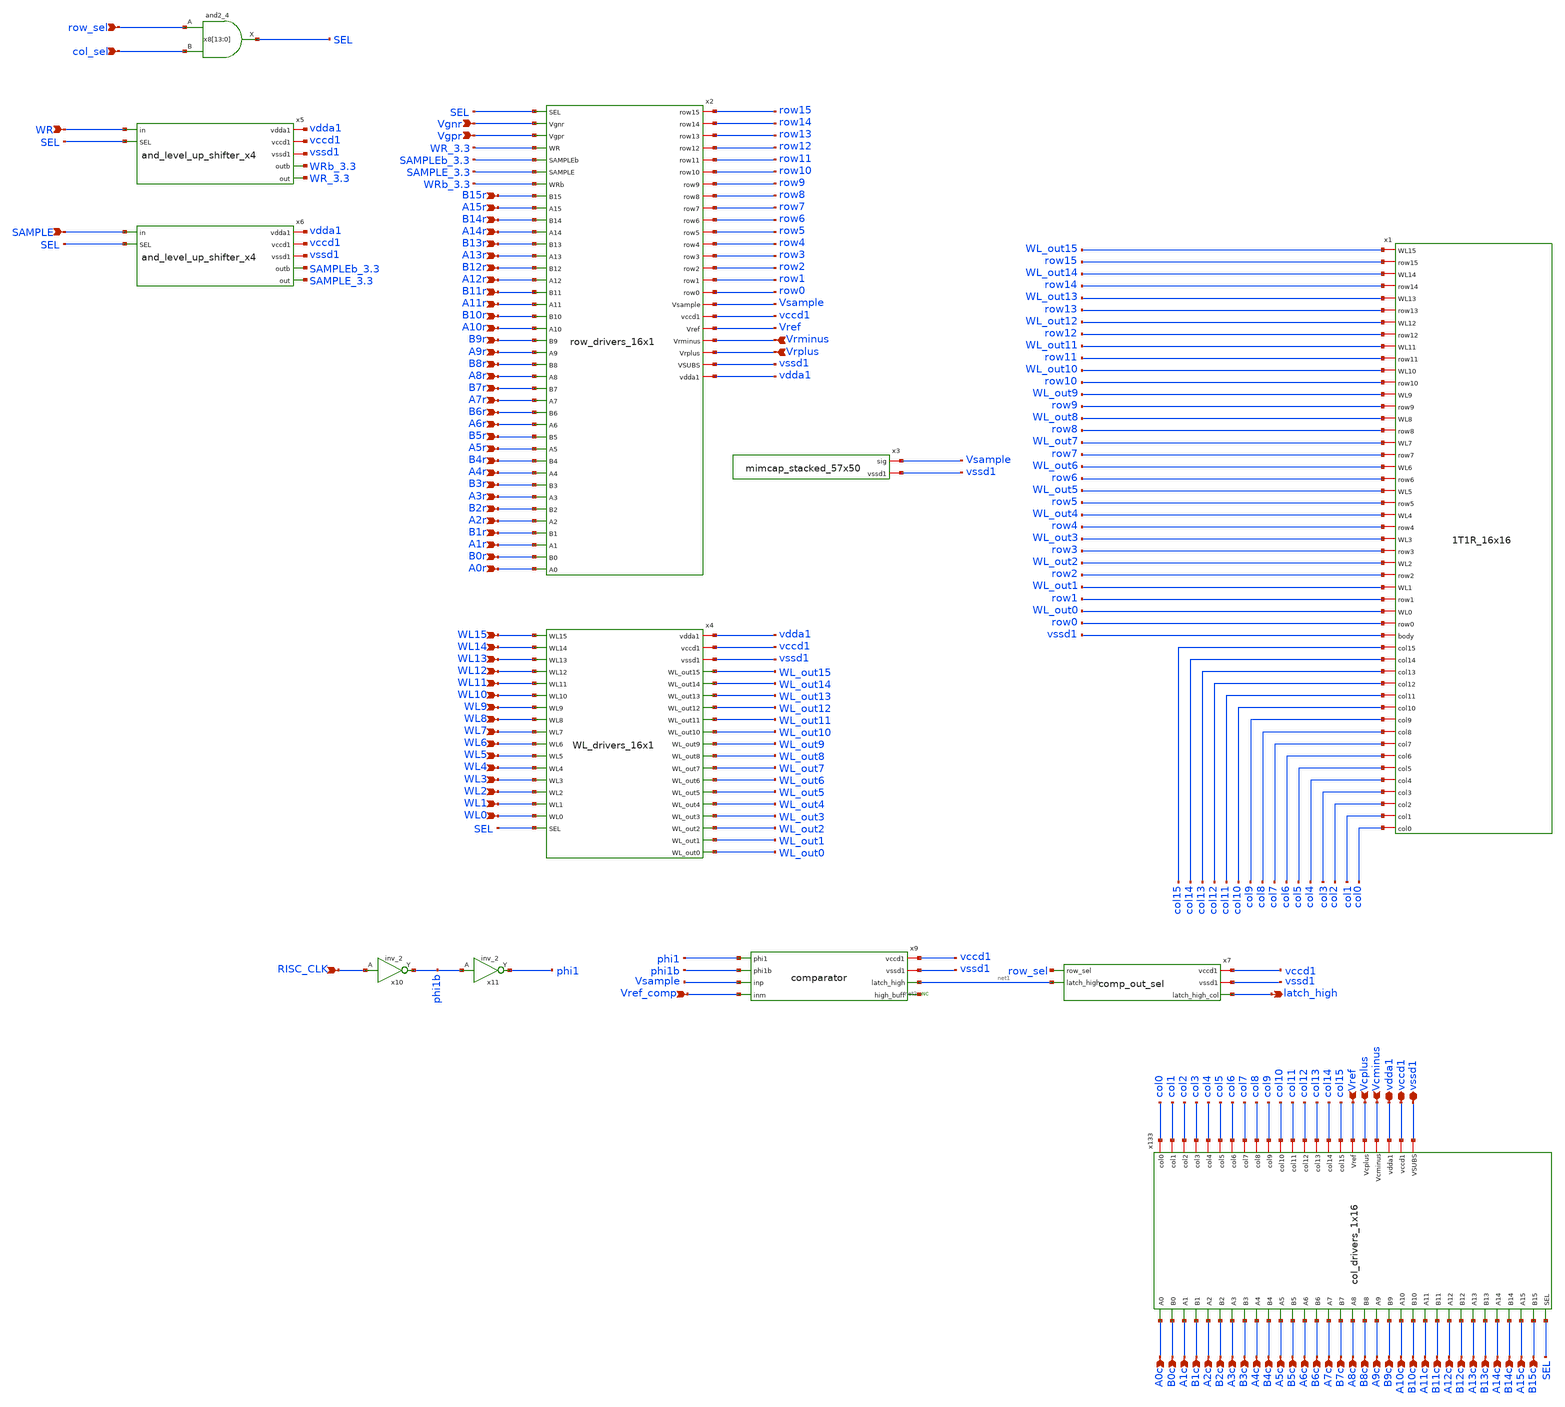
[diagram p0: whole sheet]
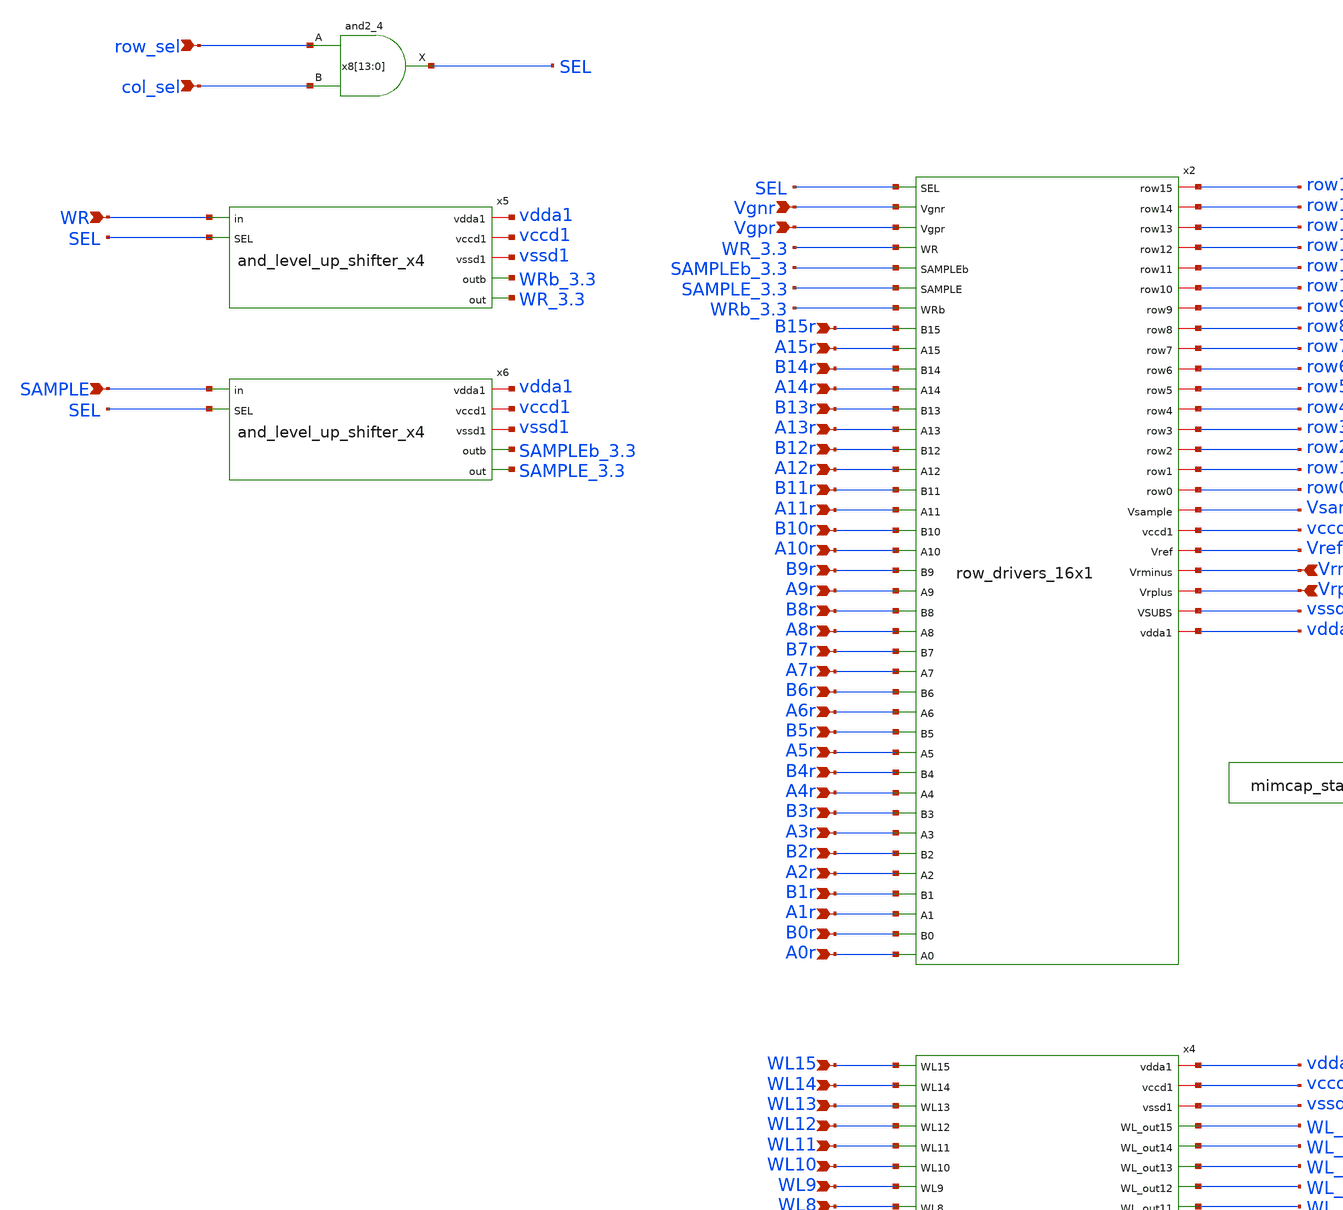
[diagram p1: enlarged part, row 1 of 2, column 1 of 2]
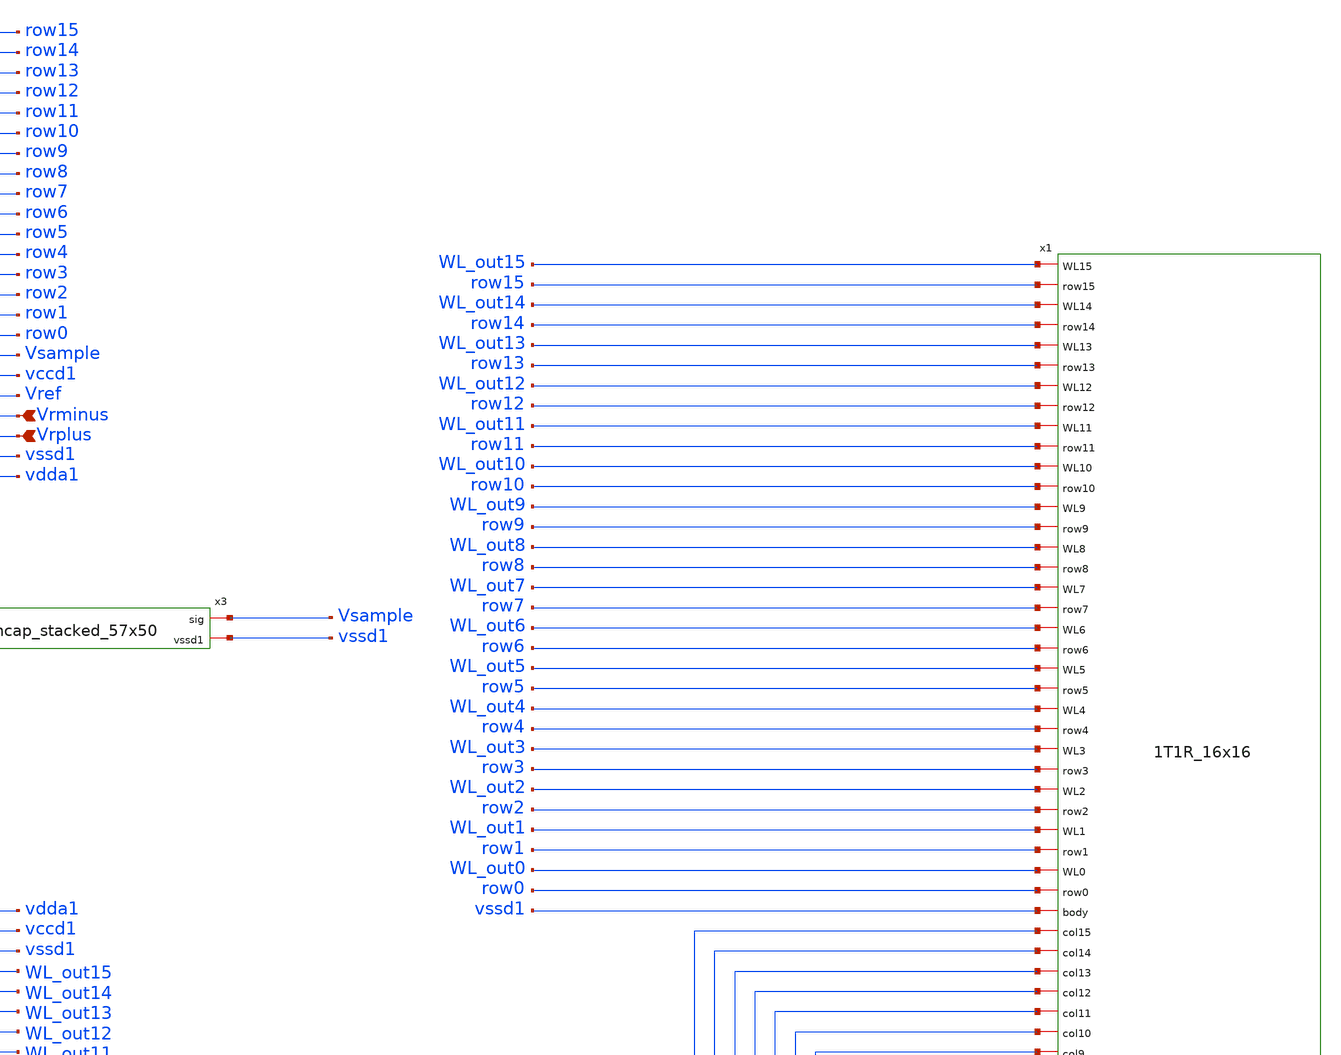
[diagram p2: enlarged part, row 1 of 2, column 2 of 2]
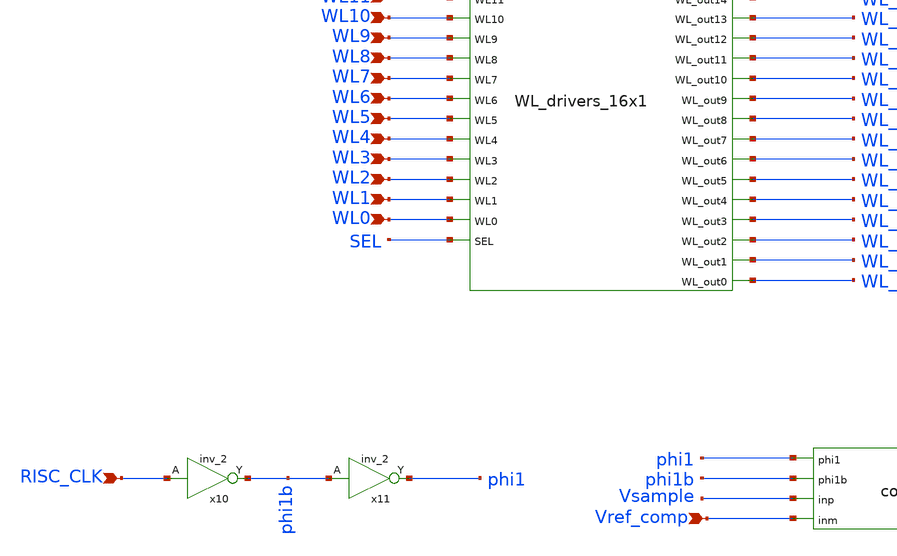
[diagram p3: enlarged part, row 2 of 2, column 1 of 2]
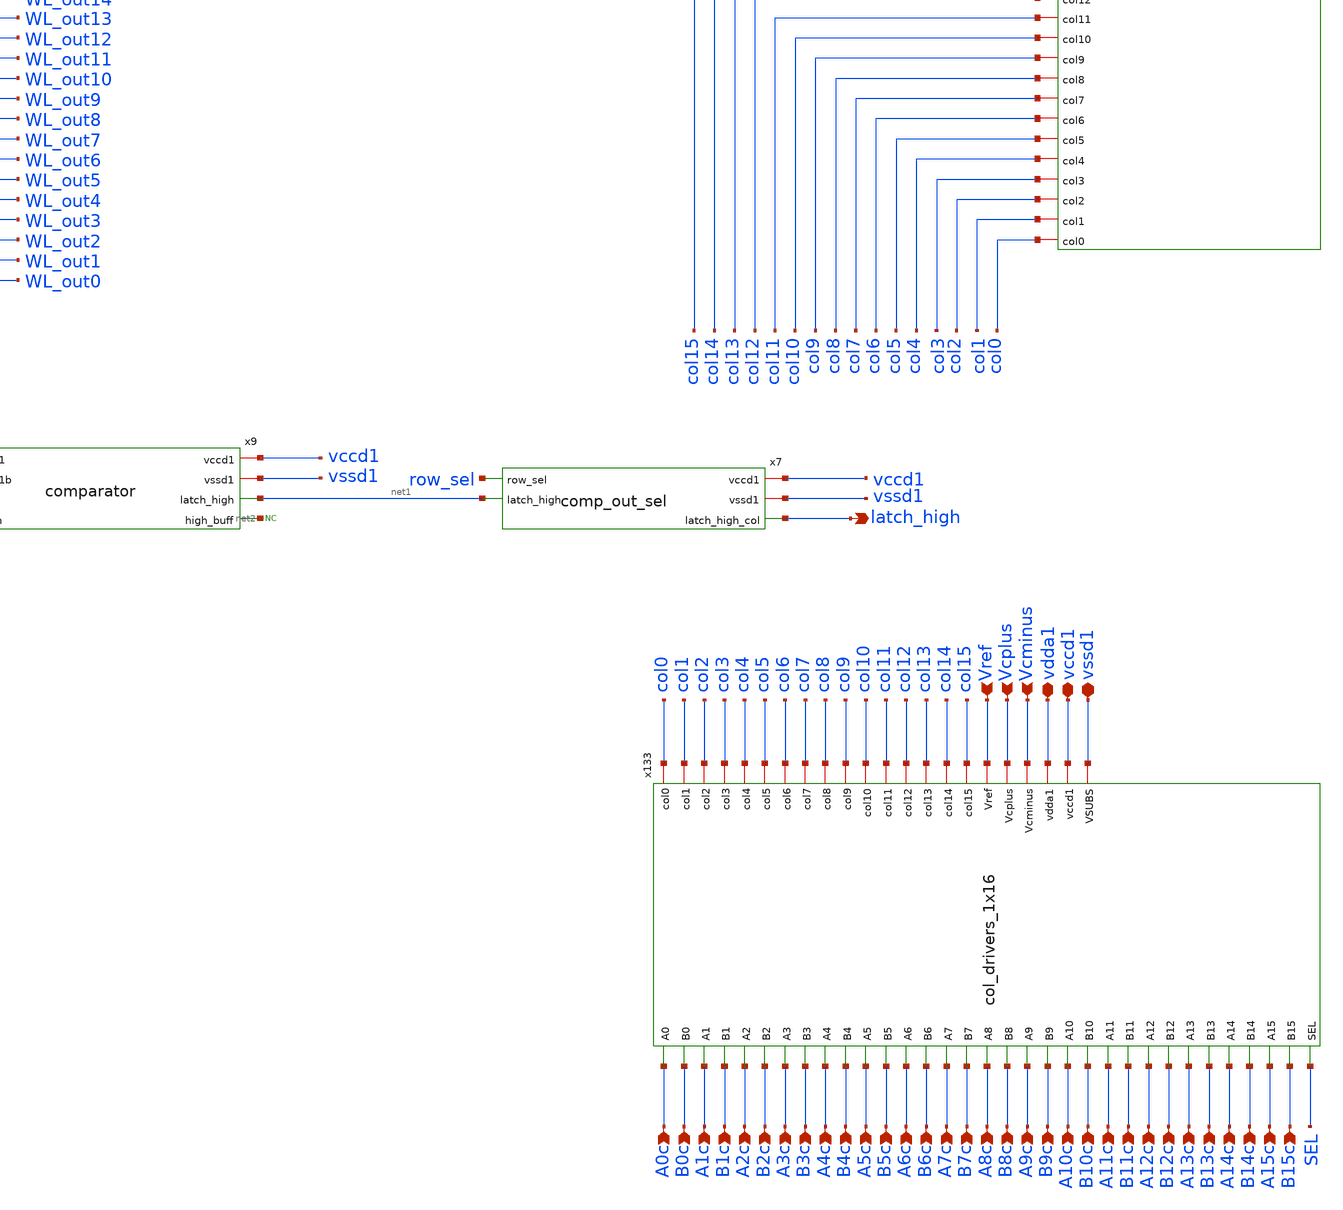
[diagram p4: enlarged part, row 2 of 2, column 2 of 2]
** sch_path: xschem/core.sch
**.subckt core vdda1 vssd1 Vref Vcplus Vcminus vccd1 Vrplus Vrminus Vgpr A0r A1r A2r A3r A4r A5r A6r
*+ A7r A8r A9r A10r A11r A12r A13r A14r A15r B0r B1r B2r B3r B4r B5r B6r B7r B8r B10r B11r B12r B13r B14r
*+ B15r B9r Vgnr A0c A1c A2c A3c A4c A5c A6c A7c A8c A9c A10c A11c A12c A13c A14c A15c B0c B1c B2c B3c B4c
*+ B5c B6c B7c B8c B10c B11c B12c B13c B14c B15c B9c WL0 WL1 WL2 WL3 WL4 WL5 WL6 WL7 WL8 WL9 WL10 WL11
*+ WL12 WL13 WL14 WL15 WR SAMPLE row_sel col_sel Vref_comp latch_high RISC_CLK
*.iopin vdda1
*.iopin vssd1
*.ipin Vref
*.ipin Vcplus
*.ipin Vcminus
*.iopin vccd1
*.ipin Vrplus
*.ipin Vrminus
*.ipin Vgpr
*.ipin A0r
*.ipin A1r
*.ipin A2r
*.ipin A3r
*.ipin A4r
*.ipin A5r
*.ipin A6r
*.ipin A7r
*.ipin A8r
*.ipin A9r
*.ipin A10r
*.ipin A11r
*.ipin A12r
*.ipin A13r
*.ipin A14r
*.ipin A15r
*.ipin B0r
*.ipin B1r
*.ipin B2r
*.ipin B3r
*.ipin B4r
*.ipin B5r
*.ipin B6r
*.ipin B7r
*.ipin B8r
*.ipin B10r
*.ipin B11r
*.ipin B12r
*.ipin B13r
*.ipin B14r
*.ipin B15r
*.ipin B9r
*.ipin Vgnr
*.ipin A0c
*.ipin A1c
*.ipin A2c
*.ipin A3c
*.ipin A4c
*.ipin A5c
*.ipin A6c
*.ipin A7c
*.ipin A8c
*.ipin A9c
*.ipin A10c
*.ipin A11c
*.ipin A12c
*.ipin A13c
*.ipin A14c
*.ipin A15c
*.ipin B0c
*.ipin B1c
*.ipin B2c
*.ipin B3c
*.ipin B4c
*.ipin B5c
*.ipin B6c
*.ipin B7c
*.ipin B8c
*.ipin B10c
*.ipin B11c
*.ipin B12c
*.ipin B13c
*.ipin B14c
*.ipin B15c
*.ipin B9c
*.ipin WL0
*.ipin WL1
*.ipin WL2
*.ipin WL3
*.ipin WL4
*.ipin WL5
*.ipin WL6
*.ipin WL7
*.ipin WL8
*.ipin WL9
*.ipin WL10
*.ipin WL11
*.ipin WL12
*.ipin WL13
*.ipin WL14
*.ipin WL15
*.ipin WR
*.ipin SAMPLE
*.ipin row_sel
*.ipin col_sel
*.ipin Vref_comp
*.opin latch_high
*.ipin RISC_CLK
x1 WL_out15 row15 WL_out14 row14 WL_out13 row13 WL_out12 row12 WL_out11 row11 WL_out10 row10 WL_out9
+ row9 WL_out8 row8 WL_out7 row7 WL_out6 row6 WL_out5 row5 WL_out4 row4 WL_out3 row3 WL_out2 row2 vssd1
+ WL_out1 row1 WL_out0 row0 col14 col15 col6 col7 col4 col11 col5 col8 col9 col2 col10 col13 col12 col3 col0
+ col1 1T1R_16x16
x133 col5 col10 col1 col4 col2 col9 col12 col13 col11 col14 col7 col0 col8 col3 col6 col15 Vref
+ Vcplus Vcminus vdda1 vccd1 vssd1 B2c A7c A2c B6c A15c A6c B7c A14c B13c B5c B1c A13c A12c A5c B4c A4c A1c
+ B10c A11c B11c A10c B12c B9c B3c A9c B8c A8c B14c A3c B0c B15c SEL A0c col_drivers_1x16
x2 SEL Vgnr Vgpr WR_3.3 SAMPLEb_3.3 SAMPLE_3.3 WRb_3.3 row15 B15r A15r row14 B14r A14r row13 B13r
+ A13r row12 B12r A12r row11 B11r A11r row10 B10r A10r row9 B9r A9r row8 B8r A8r row7 B7r A7r row6 B6r A6r
+ row5 B5r A5r row4 B4r A4r row3 B3r A3r row2 B2r A2r row1 B1r A1r row0 B0r A0r Vsample vccd1 Vref Vrminus
+ Vrplus vssd1 vdda1 row_drivers_16x1
x3 Vsample vssd1 mimcap_stacked_57x50
x4 vdda1 vccd1 vssd1 WL15 WL_out15 WL14 WL_out14 WL13 WL_out13 WL12 WL_out12 WL11 WL_out11 WL10
+ WL_out10 WL9 WL_out9 WL8 WL_out8 WL7 WL_out7 WL6 WL_out6 WL5 WL_out5 WL4 WL_out4 WL3 WL_out3 WL2 WL_out2 WL1
+ WL_out1 WL0 SEL WL_out0 WL_drivers_16x1
x5 vdda1 vccd1 vssd1 WR SEL WRb_3.3 WR_3.3 and_level_up_shifter_x4
x6 vdda1 vccd1 vssd1 SAMPLE SEL SAMPLEb_3.3 SAMPLE_3.3 and_level_up_shifter_x4
x9 vccd1 vssd1 phi1 phi1b Vsample Vref_comp net1 net2 comparator
* noconn #net2
x10 RISC_CLK vssd1 vssd1 vccd1 vccd1 phi1b sky130_fd_sc_hd__inv_2
x11 phi1b vssd1 vssd1 vccd1 vccd1 phi1 sky130_fd_sc_hd__inv_2
x8[13] row_sel col_sel vssd1 vssd1 vccd1 vccd1 SEL sky130_fd_sc_hd__and2_4
x8[12] row_sel col_sel vssd1 vssd1 vccd1 vccd1 SEL sky130_fd_sc_hd__and2_4
x8[11] row_sel col_sel vssd1 vssd1 vccd1 vccd1 SEL sky130_fd_sc_hd__and2_4
x8[10] row_sel col_sel vssd1 vssd1 vccd1 vccd1 SEL sky130_fd_sc_hd__and2_4
x8[9] row_sel col_sel vssd1 vssd1 vccd1 vccd1 SEL sky130_fd_sc_hd__and2_4
x8[8] row_sel col_sel vssd1 vssd1 vccd1 vccd1 SEL sky130_fd_sc_hd__and2_4
x8[7] row_sel col_sel vssd1 vssd1 vccd1 vccd1 SEL sky130_fd_sc_hd__and2_4
x8[6] row_sel col_sel vssd1 vssd1 vccd1 vccd1 SEL sky130_fd_sc_hd__and2_4
x8[5] row_sel col_sel vssd1 vssd1 vccd1 vccd1 SEL sky130_fd_sc_hd__and2_4
x8[4] row_sel col_sel vssd1 vssd1 vccd1 vccd1 SEL sky130_fd_sc_hd__and2_4
x8[3] row_sel col_sel vssd1 vssd1 vccd1 vccd1 SEL sky130_fd_sc_hd__and2_4
x8[2] row_sel col_sel vssd1 vssd1 vccd1 vccd1 SEL sky130_fd_sc_hd__and2_4
x8[1] row_sel col_sel vssd1 vssd1 vccd1 vccd1 SEL sky130_fd_sc_hd__and2_4
x8[0] row_sel col_sel vssd1 vssd1 vccd1 vccd1 SEL sky130_fd_sc_hd__and2_4
x7 vccd1 vssd1 row_sel latch_high net1 comp_out_sel
**** begin user architecture code
 .lib $::SKYWATER_MODELS/sky130.lib.spice tt
.include $::SKYWATER_STDCELLS/sky130_fd_sc_hd.spice

**** end user architecture code
**.ends
.end
